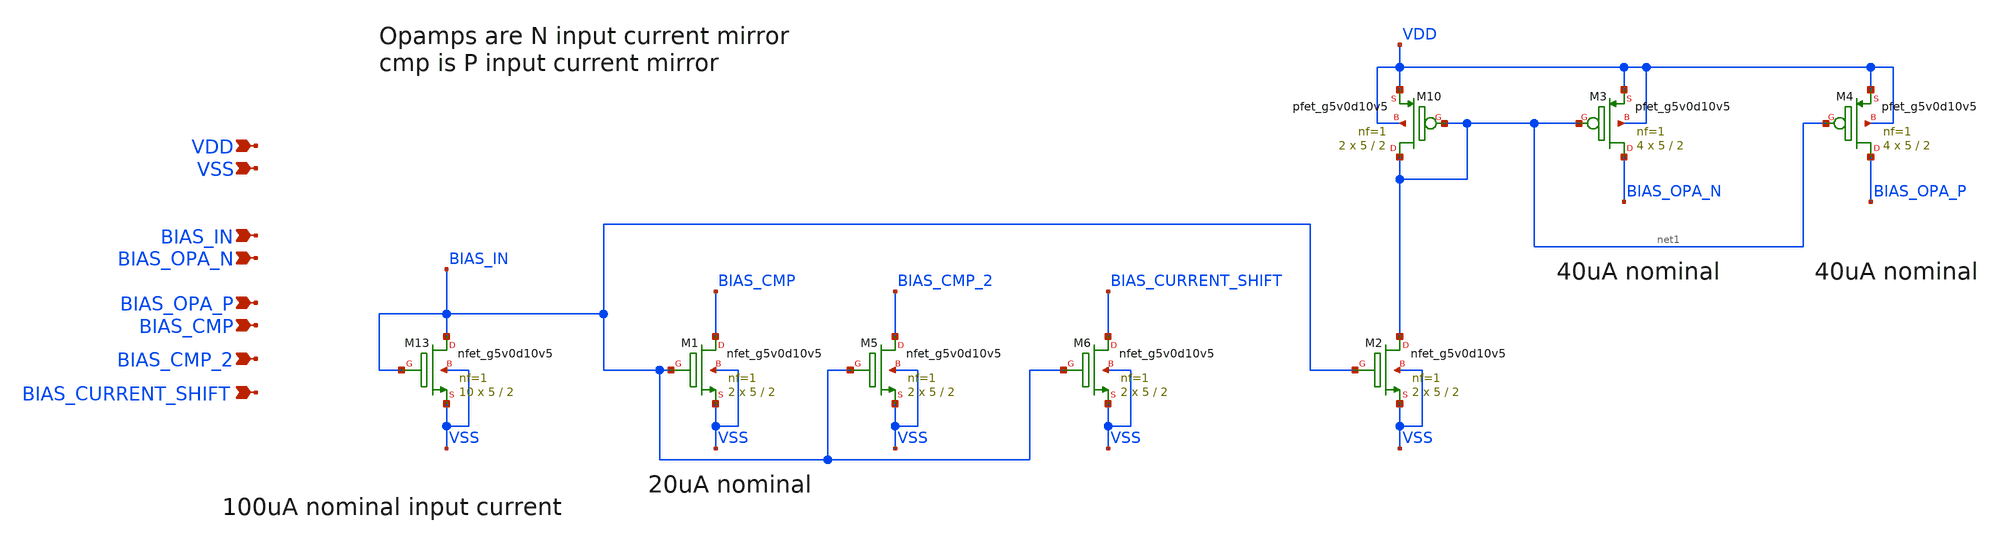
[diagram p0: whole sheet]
** sch_path: design/bias-circuit/bias_distribution.sch
**.subckt bias_distribution BIAS_OPA_P VSS VDD BIAS_IN BIAS_OPA_N BIAS_CMP BIAS_CMP_2
*+ BIAS_CURRENT_SHIFT
*.ipin BIAS_OPA_P
*.ipin VSS
*.ipin VDD
*.ipin BIAS_IN
*.ipin BIAS_OPA_N
*.ipin BIAS_CMP
*.ipin BIAS_CMP_2
*.ipin BIAS_CURRENT_SHIFT
XM10 net1 net1 VDD VDD sky130_fd_pr__pfet_g5v0d10v5 L=2 W=5 nf=1 ad='int((nf+1)/2) * W/nf * 0.29' as='int((nf+2)/2) * W/nf * 0.29'
+ pd='2*int((nf+1)/2) * (W/nf + 0.29)' ps='2*int((nf+2)/2) * (W/nf + 0.29)' nrd='0.29 / W' nrs='0.29 / W'
+ sa=0 sb=0 sd=0 mult=2 m=2
XM13 BIAS_IN BIAS_IN VSS VSS sky130_fd_pr__nfet_g5v0d10v5 L=2 W=5 nf=1 ad='int((nf+1)/2) * W/nf * 0.29'
+ as='int((nf+2)/2) * W/nf * 0.29' pd='2*int((nf+1)/2) * (W/nf + 0.29)' ps='2*int((nf+2)/2) * (W/nf + 0.29)'
+ nrd='0.29 / W' nrs='0.29 / W' sa=0 sb=0 sd=0 mult=10 m=10
XM1 BIAS_CMP BIAS_IN VSS VSS sky130_fd_pr__nfet_g5v0d10v5 L=2 W=5 nf=1 ad='int((nf+1)/2) * W/nf * 0.29'
+ as='int((nf+2)/2) * W/nf * 0.29' pd='2*int((nf+1)/2) * (W/nf + 0.29)' ps='2*int((nf+2)/2) * (W/nf + 0.29)'
+ nrd='0.29 / W' nrs='0.29 / W' sa=0 sb=0 sd=0 mult=2 m=2
XM2 net1 BIAS_IN VSS VSS sky130_fd_pr__nfet_g5v0d10v5 L=2 W=5 nf=1 ad='int((nf+1)/2) * W/nf * 0.29' as='int((nf+2)/2) * W/nf * 0.29'
+ pd='2*int((nf+1)/2) * (W/nf + 0.29)' ps='2*int((nf+2)/2) * (W/nf + 0.29)' nrd='0.29 / W' nrs='0.29 / W'
+ sa=0 sb=0 sd=0 mult=2 m=2
XM3 BIAS_OPA_N net1 VDD VDD sky130_fd_pr__pfet_g5v0d10v5 L=2 W=5 nf=1 ad='int((nf+1)/2) * W/nf * 0.29'
+ as='int((nf+2)/2) * W/nf * 0.29' pd='2*int((nf+1)/2) * (W/nf + 0.29)' ps='2*int((nf+2)/2) * (W/nf + 0.29)'
+ nrd='0.29 / W' nrs='0.29 / W' sa=0 sb=0 sd=0 mult=4 m=4
XM4 BIAS_OPA_P net1 VDD VDD sky130_fd_pr__pfet_g5v0d10v5 L=2 W=5 nf=1 ad='int((nf+1)/2) * W/nf * 0.29'
+ as='int((nf+2)/2) * W/nf * 0.29' pd='2*int((nf+1)/2) * (W/nf + 0.29)' ps='2*int((nf+2)/2) * (W/nf + 0.29)'
+ nrd='0.29 / W' nrs='0.29 / W' sa=0 sb=0 sd=0 mult=4 m=4
XM5 BIAS_CMP_2 BIAS_IN VSS VSS sky130_fd_pr__nfet_g5v0d10v5 L=2 W=5 nf=1 ad='int((nf+1)/2) * W/nf * 0.29'
+ as='int((nf+2)/2) * W/nf * 0.29' pd='2*int((nf+1)/2) * (W/nf + 0.29)' ps='2*int((nf+2)/2) * (W/nf + 0.29)'
+ nrd='0.29 / W' nrs='0.29 / W' sa=0 sb=0 sd=0 mult=2 m=2
XM6 BIAS_CURRENT_SHIFT BIAS_IN VSS VSS sky130_fd_pr__nfet_g5v0d10v5 L=2 W=5 nf=1 ad='int((nf+1)/2) * W/nf * 0.29'
+ as='int((nf+2)/2) * W/nf * 0.29' pd='2*int((nf+1)/2) * (W/nf + 0.29)' ps='2*int((nf+2)/2) * (W/nf + 0.29)'
+ nrd='0.29 / W' nrs='0.29 / W' sa=0 sb=0 sd=0 mult=2 m=2
**.ends
.end
